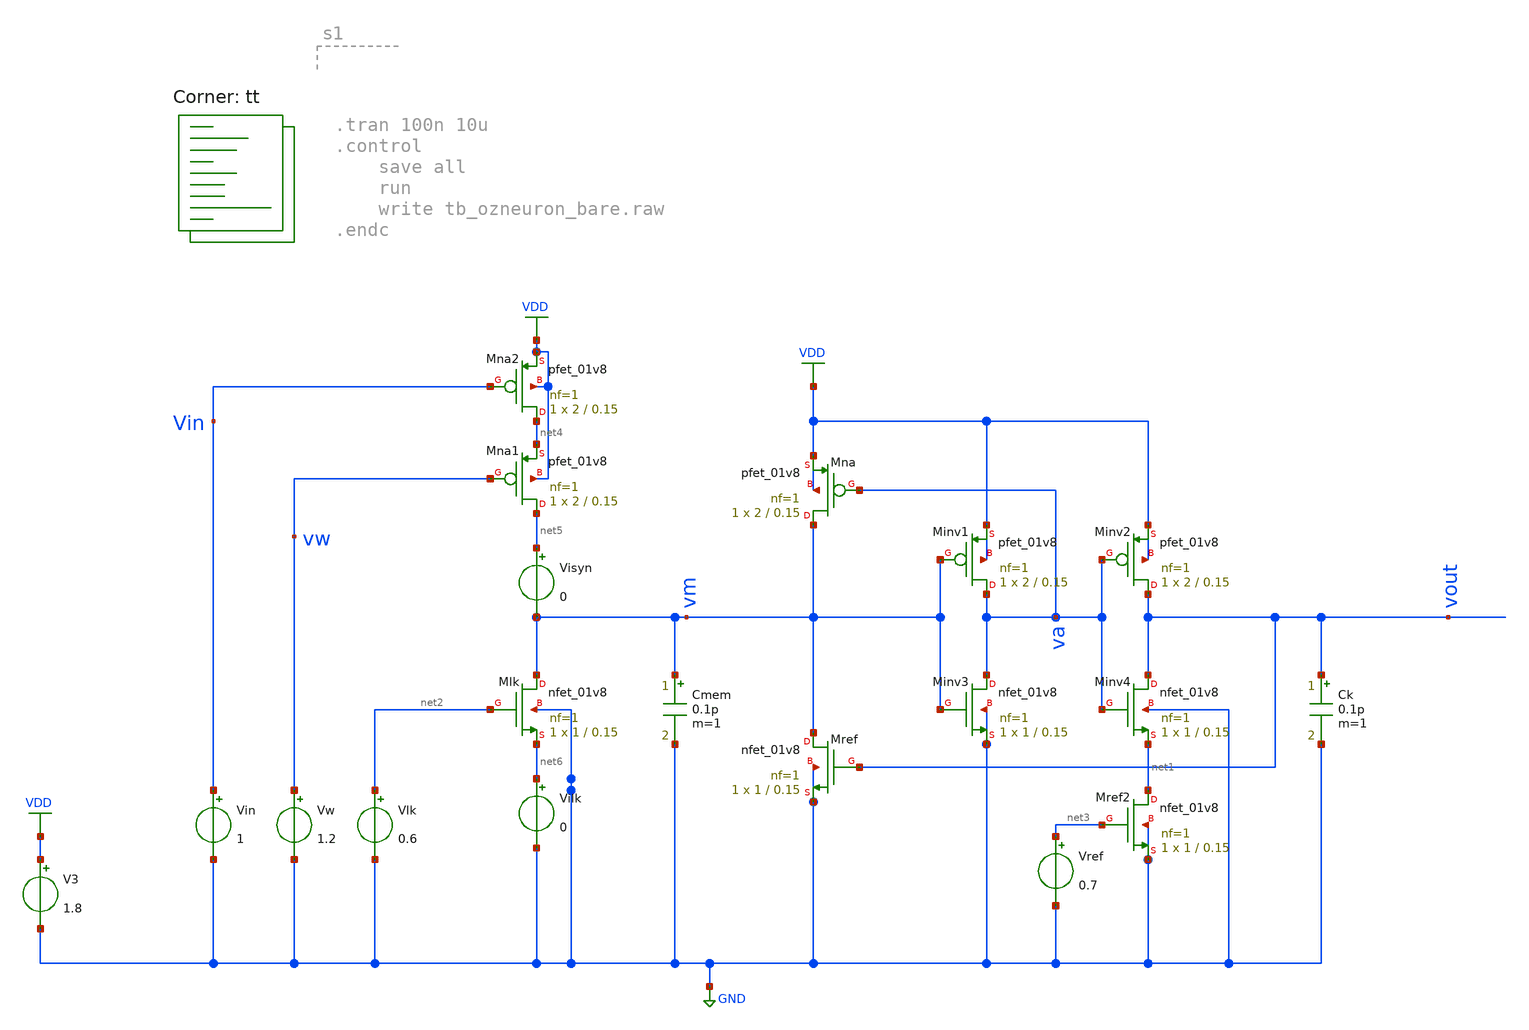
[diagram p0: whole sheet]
** sch_path: Neuron/OZNeuron/tb_ozneuron_bare.sch
**.subckt tb_ozneuron_bare
XMna vm va VDD VDD sky130_fd_pr__pfet_01v8 L=0.15 W=2 nf=1 ad='int((nf+1)/2) * W/nf * 0.29' as='int((nf+2)/2) * W/nf * 0.29'
+ pd='2*int((nf+1)/2) * (W/nf + 0.29)' ps='2*int((nf+2)/2) * (W/nf + 0.29)' nrd='0.29 / W' nrs='0.29 / W'
+ sa=0 sb=0 sd=0 mult=1 m=1
XMlk vm net2 net6 GND sky130_fd_pr__nfet_01v8 L=0.15 W=1 nf=1 ad='int((1 + 1)/2) * 1 / 1 * 0.29' as='int((1 + 2)/2) * 1 / 1 * 0.29'
+ pd='2*int((1 + 1)/2) * (1 / 1 + 0.29)' ps='2*int((1 + 2)/2) * (1 / 1 + 0.29)' nrd='0.29 / 1 ' nrs='0.29 / 1 '
+ sa=0 sb=0 sd=0 mult=1 m=1
XMinv1 va vm VDD VDD sky130_fd_pr__pfet_01v8 L=0.15 W=2 nf=1 ad='int((nf+1)/2) * W/nf * 0.29' as='int((nf+2)/2) * W/nf * 0.29'
+ pd='2*int((nf+1)/2) * (W/nf + 0.29)' ps='2*int((nf+2)/2) * (W/nf + 0.29)' nrd='0.29 / W' nrs='0.29 / W'
+ sa=0 sb=0 sd=0 mult=1 m=1
XMinv2 vout va VDD VDD sky130_fd_pr__pfet_01v8 L=0.15 W=2 nf=1 ad='int((nf+1)/2) * W/nf * 0.29' as='int((nf+2)/2) * W/nf * 0.29'
+ pd='2*int((nf+1)/2) * (W/nf + 0.29)' ps='2*int((nf+2)/2) * (W/nf + 0.29)' nrd='0.29 / W' nrs='0.29 / W'
+ sa=0 sb=0 sd=0 mult=1 m=1
XMref vm vout GND GND sky130_fd_pr__nfet_01v8 L=0.15 W=1 nf=1 ad='int((1 + 1)/2) * 1 / 1 * 0.29' as='int((1 + 2)/2) * 1 / 1 * 0.29'
+ pd='2*int((1 + 1)/2) * (1 / 1 + 0.29)' ps='2*int((1 + 2)/2) * (1 / 1 + 0.29)' nrd='0.29 / 1 ' nrs='0.29 / 1 '
+ sa=0 sb=0 sd=0 mult=1 m=1
XMinv3 va vm GND GND sky130_fd_pr__nfet_01v8 L=0.15 W=1 nf=1 ad='int((1 + 1)/2) * 1 / 1 * 0.29' as='int((1 + 2)/2) * 1 / 1 * 0.29'
+ pd='2*int((1 + 1)/2) * (1 / 1 + 0.29)' ps='2*int((1 + 2)/2) * (1 / 1 + 0.29)' nrd='0.29 / 1 ' nrs='0.29 / 1 '
+ sa=0 sb=0 sd=0 mult=1 m=1
XMinv4 vout va net1 GND sky130_fd_pr__nfet_01v8 L=0.15 W=1 nf=1 ad='int((1 + 1)/2) * 1 / 1 * 0.29' as='int((1 + 2)/2) * 1 / 1 * 0.29'
+ pd='2*int((1 + 1)/2) * (1 / 1 + 0.29)' ps='2*int((1 + 2)/2) * (1 / 1 + 0.29)' nrd='0.29 / 1 ' nrs='0.29 / 1 '
+ sa=0 sb=0 sd=0 mult=1 m=1
XMref2 net1 net3 GND GND sky130_fd_pr__nfet_01v8 L=0.15 W=1 nf=1 ad='int((1 + 1)/2) * 1 / 1 * 0.29' as='int((1 + 2)/2) * 1 / 1 * 0.29'
+ pd='2*int((1 + 1)/2) * (1 / 1 + 0.29)' ps='2*int((1 + 2)/2) * (1 / 1 + 0.29)' nrd='0.29 / 1 ' nrs='0.29 / 1 '
+ sa=0 sb=0 sd=0 mult=1 m=1
Cmem vm GND 0.1p m=1
Ck vout GND 0.1p m=1
Vlk net2 GND 0.6
Vref net3 GND 0.7
V3 VDD GND 1.8
XMna1 net5 vw net4 VDD sky130_fd_pr__pfet_01v8 L=0.15 W=2 nf=1 ad='int((nf+1)/2) * W/nf * 0.29' as='int((nf+2)/2) * W/nf * 0.29'
+ pd='2*int((nf+1)/2) * (W/nf + 0.29)' ps='2*int((nf+2)/2) * (W/nf + 0.29)' nrd='0.29 / W' nrs='0.29 / W'
+ sa=0 sb=0 sd=0 mult=1 m=1
XMna2 net4 Vin VDD VDD sky130_fd_pr__pfet_01v8 L=0.15 W=2 nf=1 ad='int((nf+1)/2) * W/nf * 0.29' as='int((nf+2)/2) * W/nf * 0.29'
+ pd='2*int((nf+1)/2) * (W/nf + 0.29)' ps='2*int((nf+2)/2) * (W/nf + 0.29)' nrd='0.29 / W' nrs='0.29 / W'
+ sa=0 sb=0 sd=0 mult=1 m=1
Visyn net5 vm 0
.save i(visyn)
Vw vw GND 1.2
Vin Vin GND 1
Vilk net6 GND 0
.save i(vilk)
**** begin user architecture code
.lib $::SKYWATER_MODELS/sky130.lib.spice tt



.nodeset v(vm)=1
.tran 5n 10u
.control
	save all
	*set wr_singlescale
	set wr_vecnames
	option numdgt = 4
	compose Vlk_list start=0 stop=1.8 step=0.1
	compose Vin_list start=0 stop=1.8 step=0.09
    foreach vlk $&Vlk_list
        alter Vlk $vlk
        set namestr = 'tc_{$vlk}.txt'
        set writestr = ' '
        foreach vin $&Vin_list
            alter Vin $vin
            run
            set writestr = ( $writestr {$curplot}.v(vout) )
        end
	wrdata /home/alex/Desktop/EDA/SNN_IPN/Neuron/OZNeuron/sims/{$namestr} $writestr
    end
.endc


**** end user architecture code
**.ends
.GLOBAL VDD
.GLOBAL GND
.end
